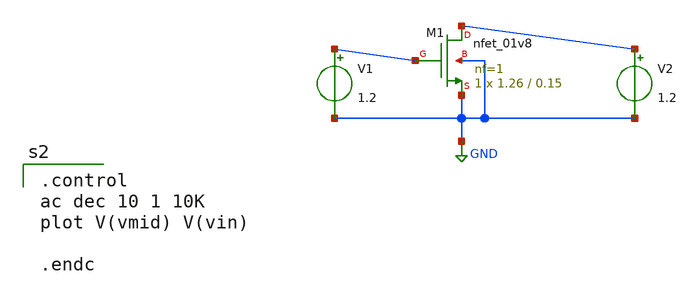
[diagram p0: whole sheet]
** sch_path: xschem/untitled-4.sch
**.subckt untitled-4
XM1 net2 net1 GND GND sky130_fd_pr__nfet_01v8 L=0.15 W=1.26 nf=1 ad='int((nf+1)/2) * W/nf * 0.29' as='int((nf+2)/2) * W/nf * 0.29'
+ pd='2*int((nf+1)/2) * (W/nf + 0.29)' ps='2*int((nf+2)/2) * (W/nf + 0.29)' nrd='0.29 / W' nrs='0.29 / W'
+ sa=0 sb=0 sd=0 mult=1 m=1
V1 net1 GND 1.2
V2 net2 GND 1.2
**** begin user architecture code
.lib $::SKYWATER_MODELS/sky130.lib.spice tt
.include $::PDKPATH/libs.ref/sky130_fd_sc_hvl/spice/sky130_fd_sc_hvl.spice

.control
ac dec 10 1 10K
plot V(vmid) V(vin)

.endc


**** end user architecture code
**.ends
.GLOBAL GND
.end
